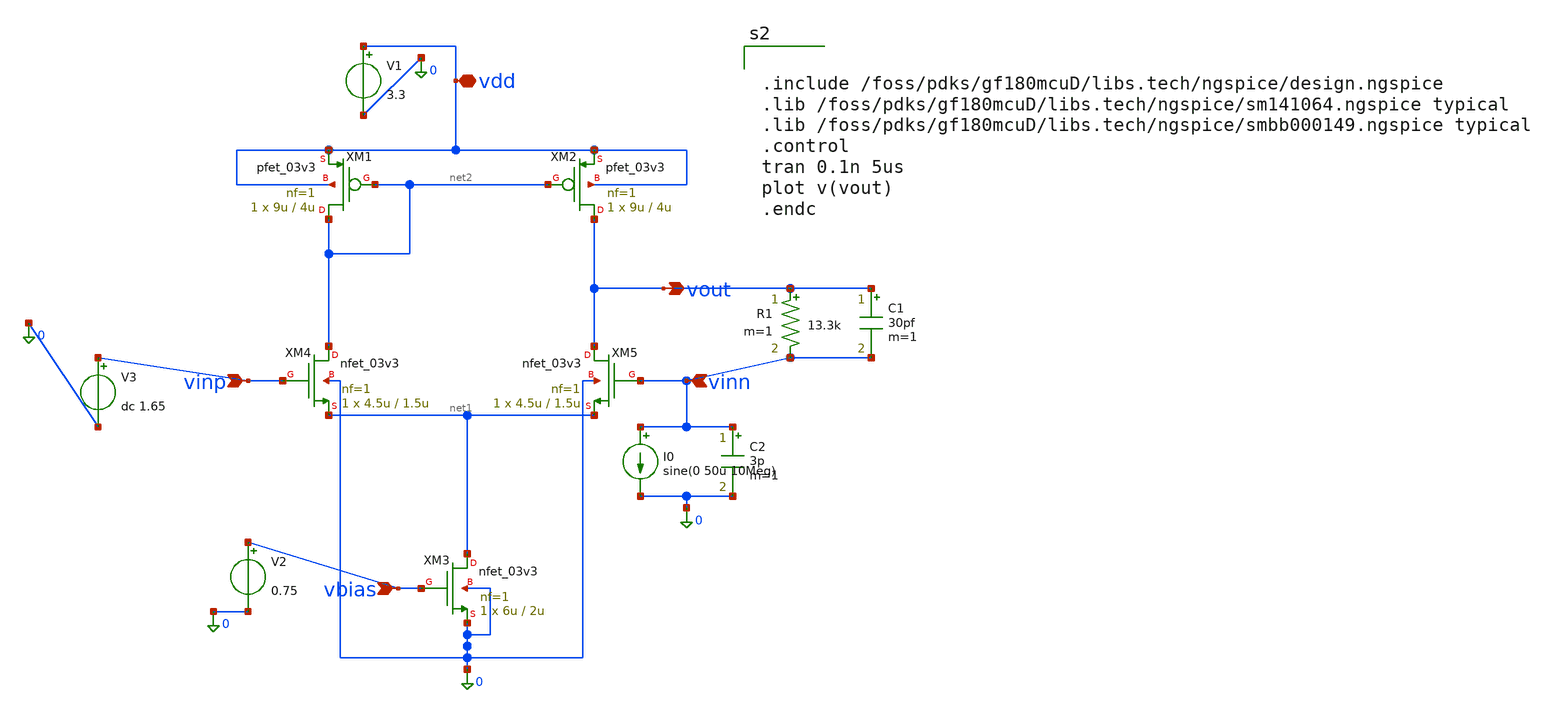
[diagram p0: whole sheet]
** sch_path: 5totawithfeedbackresistor-4.sch
**.subckt 5totawithfeedbackresistor-4 vbias vdd vinp vinn vout
*.ipin vbias
*.iopin vdd
*.ipin vinp
*.ipin vinn
*.opin vout
XM1 net2 net2 vdd vdd pfet_03v3 L=4u W=9u nf=1 ad='int((nf+1)/2) * W/nf * 0.18u' as='int((nf+2)/2) * W/nf * 0.18u'
+ pd='2*int((nf+1)/2) * (W/nf + 0.18u)' ps='2*int((nf+2)/2) * (W/nf + 0.18u)' nrd='0.18u / W' nrs='0.18u / W'
+ sa=0 sb=0 sd=0 m=1
XM3 net1 vbias 0 0 nfet_03v3 L=2u W=6u nf=1 ad='int((nf+1)/2) * W/nf * 0.18u' as='int((nf+2)/2) * W/nf * 0.18u'
+ pd='2*int((nf+1)/2) * (W/nf + 0.18u)' ps='2*int((nf+2)/2) * (W/nf + 0.18u)' nrd='0.18u / W' nrs='0.18u / W'
+ sa=0 sb=0 sd=0 m=1
XM2 vout net2 vdd vdd pfet_03v3 L=4u W=9u nf=1 ad='int((nf+1)/2) * W/nf * 0.18u' as='int((nf+2)/2) * W/nf * 0.18u'
+ pd='2*int((nf+1)/2) * (W/nf + 0.18u)' ps='2*int((nf+2)/2) * (W/nf + 0.18u)' nrd='0.18u / W' nrs='0.18u / W'
+ sa=0 sb=0 sd=0 m=1
XM4 net2 vinp net1 0 nfet_03v3 L=1.5u W=4.5u nf=1 ad='int((nf+1)/2) * W/nf * 0.18u' as='int((nf+2)/2) * W/nf * 0.18u'
+ pd='2*int((nf+1)/2) * (W/nf + 0.18u)' ps='2*int((nf+2)/2) * (W/nf + 0.18u)' nrd='0.18u / W' nrs='0.18u / W'
+ sa=0 sb=0 sd=0 m=1
XM5 vout vinn net1 0 nfet_03v3 L=1.5u W=4.5u nf=1 ad='int((nf+1)/2) * W/nf * 0.18u' as='int((nf+2)/2) * W/nf * 0.18u'
+ pd='2*int((nf+1)/2) * (W/nf + 0.18u)' ps='2*int((nf+2)/2) * (W/nf + 0.18u)' nrd='0.18u / W' nrs='0.18u / W'
+ sa=0 sb=0 sd=0 m=1
V1 vdd 0 3.3
V2 vbias 0 0.75
V3 vinp 0 dc 1.65
C1 vout vinn 30pf m=1
R1 vout vinn 13.3k m=1
I0 vinn 0 sine(0 50u 10Meg)
C2 vinn 0 3p m=1
**** begin user architecture code


.include /foss/pdks/gf180mcuD/libs.tech/ngspice/design.ngspice
.lib /foss/pdks/gf180mcuD/libs.tech/ngspice/sm141064.ngspice typical
.lib /foss/pdks/gf180mcuD/libs.tech/ngspice/smbb000149.ngspice typical
.control
tran 0.1n 5us
plot v(vout)
.endc

**** end user architecture code
**.ends
.end
